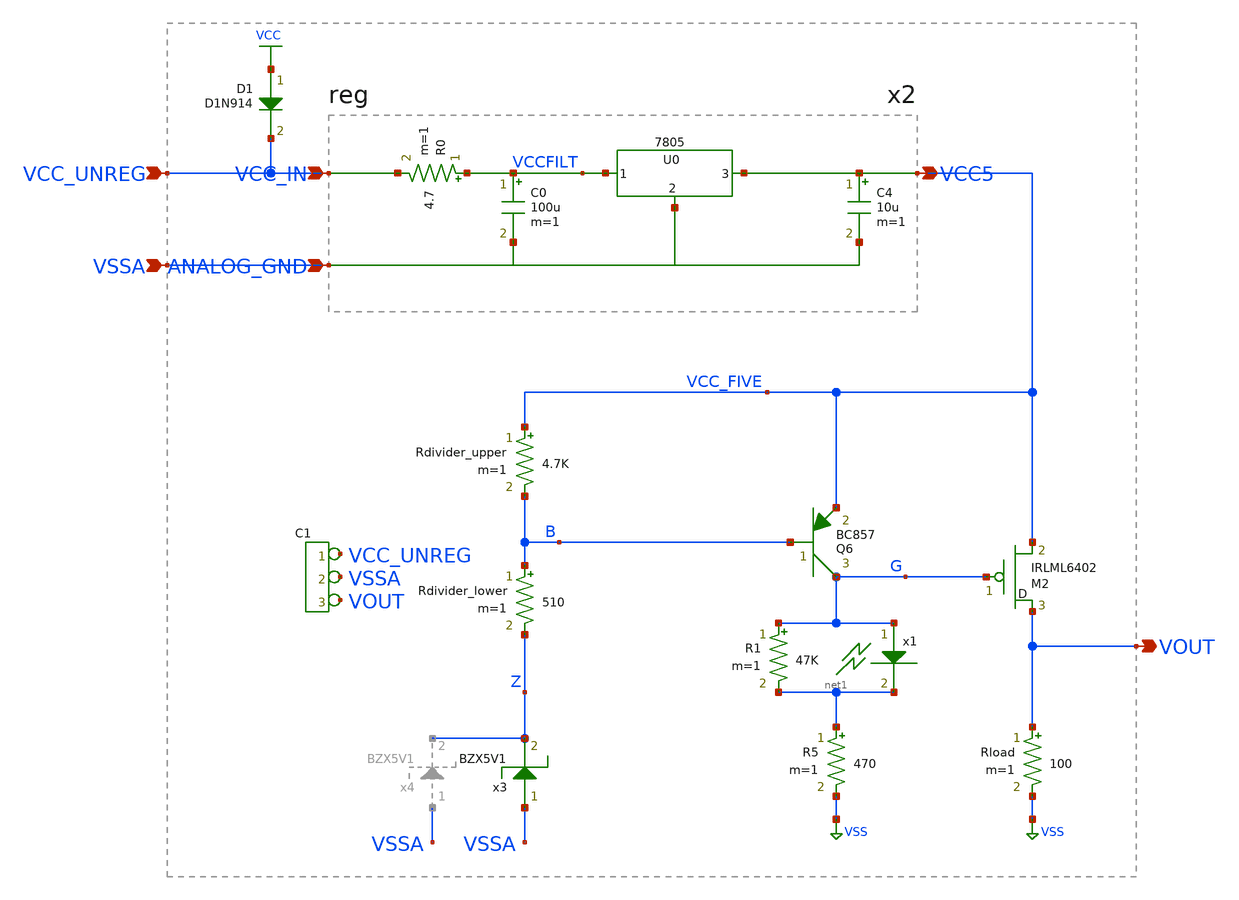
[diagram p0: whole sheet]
** sch_path: xschem-src/xschem_library/pcb/voltage_protection.sch
* Copyright (C) 1998-2026 Stefan Frederik Schippers
* This program is free software; you can redistribute it and/or modify
* it under the terms of the GNU General Public License as published by
* the Free Software Foundation; either version 2 of the License, or
* (at your option) any later version.
* This program is distributed in the hope that it will be useful,
* but WITHOUT ANY WARRANTY; without even the implied warranty of
* MERCHANTABILITY or FITNESS FOR A PARTICULAR PURPOSE.  See the
* GNU General Public License for more details.
* You should have received a copy of the GNU General Public License
* along with this program; if not, write to the Free Software
**.subckt voltage_protection VOUT VCC_UNREG VSSA
*.opin VOUT
*.ipin VCC_UNREG
*.ipin VSSA
*connector(3,1) ?1 VCC_UNREG ?1 VSSA ?1 VOUT
Rload VOUT VSS 100 m=1
Q6 G B VCC_FIVE BC857 area=1 m=1
x3 VSSA Z BZX5V1
Rdivider_upper VCC_FIVE B 4.7K m=1
R5 net1 VSS 470 m=1
Rdivider_lower B Z 510 m=1
XM2 VOUT G VCC_FIVE IRLML6402 m=1
x1 G net1 D1N5765
R1 G net1 47K m=1
x2 VCC_FIVE VCC_UNREG VSSA reg
D1 VCC VCC_UNREG D1N914 area=1
**.ends

* expanding   symbol:  reg.sch # of pins=3
** sym_path: xschem-src/xschem_library/pcb/reg.sch
** sch_path: xschem-src/xschem_library/pcb/reg.sch
.subckt reg VCC5 VCC_IN ANALOG_GND
*.opin VCC5
*.ipin VCC_IN
*.ipin ANALOG_GND
C0 VCCFILT ANALOG_GND 100u m=1
XU0 VCCFILT ANALOG_GND VCC5 7805
C4 VCC5 ANALOG_GND 10u m=1
R0 VCCFILT VCC_IN 4.7 m=1
.ends

.GLOBAL VSS
.GLOBAL VCC
.end
